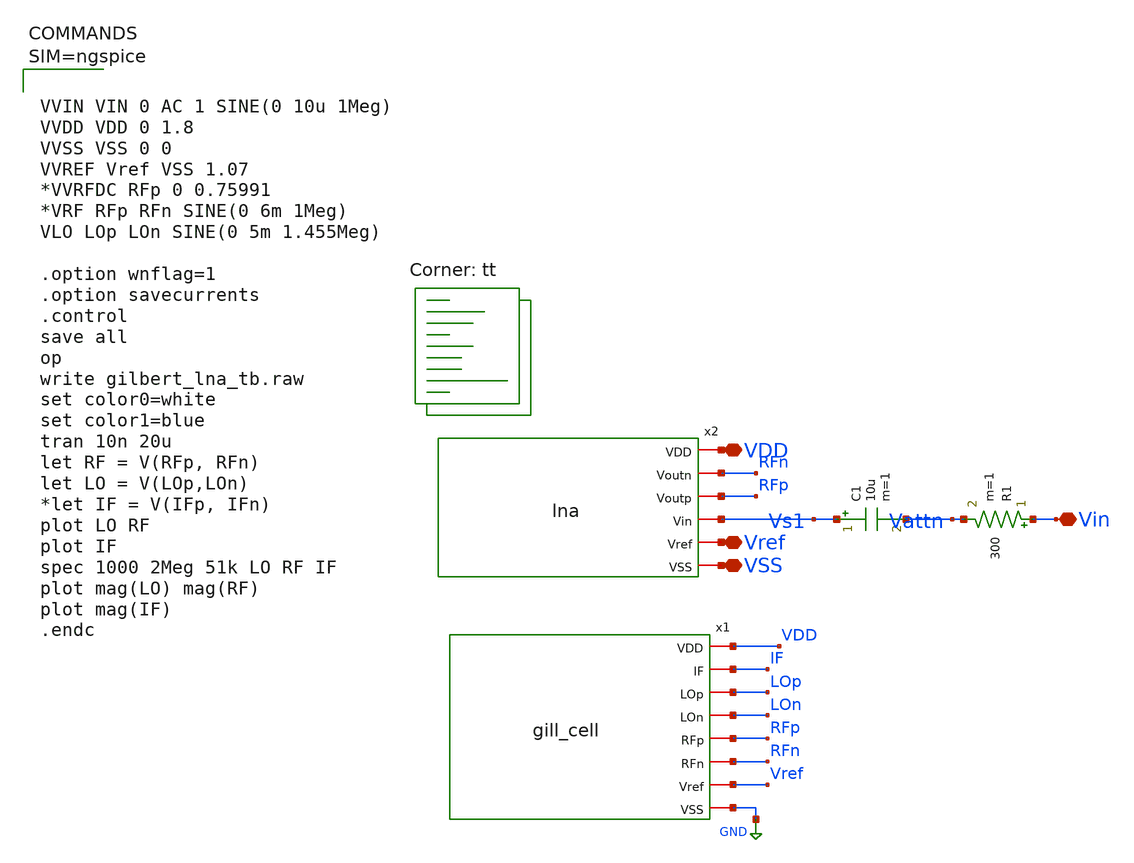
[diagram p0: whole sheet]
** sch_path: Project/xschem/gilbert_lna_tb.sch
**.subckt gilbert_lna_tb VDD Vin Vref VSS
*.iopin VDD
*.iopin Vin
*.iopin Vref
*.iopin VSS
x1 VDD IF LOp LOn RFp RFn Vref GND gill_cell
C1 Vs1 Vattn 10u m=1
R1 Vin Vattn 300 m=1
x2 VDD RFn RFp Vs1 Vref VSS lna
**** begin user architecture code



VVIN VIN 0 AC 1 SINE(0 10u 1Meg)
VVDD VDD 0 1.8
VVSS VSS 0 0
VVREF Vref VSS 1.07
*VVRFDC RFp 0 0.75991
*VRF RFp RFn SINE(0 6m 1Meg)
VLO LOp LOn SINE(0 5m 1.455Meg)

.option wnflag=1
.option savecurrents
.control
save all
op
write gilbert_lna_tb.raw
set color0=white
set color1=blue
tran 10n 20u
let RF = V(RFp, RFn)
let LO = V(LOp,LOn)
*let IF = V(IFp, IFn)
plot LO RF
plot IF
spec 1000 2Meg 51k LO RF IF
plot mag(LO) mag(RF)
plot mag(IF)
.endc



.lib $::SKYWATER_MODELS/sky130.lib.spice tt
**** end user architecture code
**.ends

* expanding   symbol:  gill_cell.sym # of pins=8
** sym_path: Project/xschem/gill_cell.sym
** sch_path: Project/xschem/gill_cell.sch
.subckt gill_cell VDD IF LOp LOn RFp RFn Vref VSS
*.iopin LOp
*.iopin LOn
*.iopin RFp
*.iopin RFn
*.iopin VDD
*.iopin VSS
*.iopin Vref
*.iopin IF
XR1 IF++ VDD VSS sky130_fd_pr__res_xhigh_po_0p69 L=6.9 mult=1 m=1
XR3 IF-- VDD VSS sky130_fd_pr__res_xhigh_po_0p69 L=6.9 mult=1 m=1
XR10 VDD LOp VSS sky130_fd_pr__res_xhigh_po_0p69 L=1.38 mult=1 m=1
XR11 LOp VSS VSS sky130_fd_pr__res_xhigh_po_0p69 L=3.45 mult=1 m=1
XR12 LOn VDD VSS sky130_fd_pr__res_xhigh_po_0p69 L=1.38 mult=1 m=1
XR13 VSS LOn VSS sky130_fd_pr__res_xhigh_po_0p69 L=3.45 mult=1 m=1
XM2 net1 VM VSS VSS sky130_fd_pr__nfet_01v8 L=1.1 W=40 nf=1 ad='int((nf+1)/2) * W/nf * 0.29' as='int((nf+2)/2) * W/nf * 0.29'
+ pd='2*int((nf+1)/2) * (W/nf + 0.29)' ps='2*int((nf+2)/2) * (W/nf + 0.29)' nrd='0.29 / W' nrs='0.29 / W'
+ sa=0 sb=0 sd=0 mult=1 m=1
XM3 Vmid RFp net1 VSS sky130_fd_pr__nfet_01v8 L=1.1 W=40 nf=1 ad='int((nf+1)/2) * W/nf * 0.29' as='int((nf+2)/2) * W/nf * 0.29'
+ pd='2*int((nf+1)/2) * (W/nf + 0.29)' ps='2*int((nf+2)/2) * (W/nf + 0.29)' nrd='0.29 / W' nrs='0.29 / W'
+ sa=0 sb=0 sd=0 mult=1 m=1
XM5 IF++ LOp Vmid VSS sky130_fd_pr__nfet_01v8 L=1.1 W=40 nf=1 ad='int((nf+1)/2) * W/nf * 0.29' as='int((nf+2)/2) * W/nf * 0.29'
+ pd='2*int((nf+1)/2) * (W/nf + 0.29)' ps='2*int((nf+2)/2) * (W/nf + 0.29)' nrd='0.29 / W' nrs='0.29 / W'
+ sa=0 sb=0 sd=0 mult=1 m=1
XM7 IF++ LOn Vmid2 VSS sky130_fd_pr__nfet_01v8 L=1.1 W=40 nf=1 ad='int((nf+1)/2) * W/nf * 0.29' as='int((nf+2)/2) * W/nf * 0.29'
+ pd='2*int((nf+1)/2) * (W/nf + 0.29)' ps='2*int((nf+2)/2) * (W/nf + 0.29)' nrd='0.29 / W' nrs='0.29 / W'
+ sa=0 sb=0 sd=0 mult=1 m=1
XM4 Vmid2 RFn net1 VSS sky130_fd_pr__nfet_01v8 L=1.1 W=40 nf=1 ad='int((nf+1)/2) * W/nf * 0.29' as='int((nf+2)/2) * W/nf * 0.29'
+ pd='2*int((nf+1)/2) * (W/nf + 0.29)' ps='2*int((nf+2)/2) * (W/nf + 0.29)' nrd='0.29 / W' nrs='0.29 / W'
+ sa=0 sb=0 sd=0 mult=1 m=1
XM8 IF-- LOp Vmid2 VSS sky130_fd_pr__nfet_01v8 L=1.1 W=40 nf=1 ad='int((nf+1)/2) * W/nf * 0.29' as='int((nf+2)/2) * W/nf * 0.29'
+ pd='2*int((nf+1)/2) * (W/nf + 0.29)' ps='2*int((nf+2)/2) * (W/nf + 0.29)' nrd='0.29 / W' nrs='0.29 / W'
+ sa=0 sb=0 sd=0 mult=1 m=1
XM6 IF-- LOn Vmid VSS sky130_fd_pr__nfet_01v8 L=1.1 W=40 nf=1 ad='int((nf+1)/2) * W/nf * 0.29' as='int((nf+2)/2) * W/nf * 0.29'
+ pd='2*int((nf+1)/2) * (W/nf + 0.29)' ps='2*int((nf+2)/2) * (W/nf + 0.29)' nrd='0.29 / W' nrs='0.29 / W'
+ sa=0 sb=0 sd=0 mult=1 m=1
XM9 Vamp VM VSS VSS sky130_fd_pr__nfet_01v8 L=1.1 W=40 nf=1 ad='int((nf+1)/2) * W/nf * 0.29' as='int((nf+2)/2) * W/nf * 0.29'
+ pd='2*int((nf+1)/2) * (W/nf + 0.29)' ps='2*int((nf+2)/2) * (W/nf + 0.29)' nrd='0.29 / W' nrs='0.29 / W'
+ sa=0 sb=0 sd=0 mult=1 m=1
XM10 IFn IF++ Vamp VSS sky130_fd_pr__nfet_01v8 L=1.1 W=40 nf=1 ad='int((nf+1)/2) * W/nf * 0.29' as='int((nf+2)/2) * W/nf * 0.29'
+ pd='2*int((nf+1)/2) * (W/nf + 0.29)' ps='2*int((nf+2)/2) * (W/nf + 0.29)' nrd='0.29 / W' nrs='0.29 / W'
+ sa=0 sb=0 sd=0 mult=1 m=1
XM11 IFp IF-- Vamp VSS sky130_fd_pr__nfet_01v8 L=1.1 W=40 nf=1 ad='int((nf+1)/2) * W/nf * 0.29' as='int((nf+2)/2) * W/nf * 0.29'
+ pd='2*int((nf+1)/2) * (W/nf + 0.29)' ps='2*int((nf+2)/2) * (W/nf + 0.29)' nrd='0.29 / W' nrs='0.29 / W'
+ sa=0 sb=0 sd=0 mult=1 m=1
XR14 IFp VDD VSS sky130_fd_pr__res_xhigh_po_0p69 L=9.67 mult=1 m=1
XR15 IFn VDD VSS sky130_fd_pr__res_xhigh_po_0p69 L=9.67 mult=1 m=1
XM1 net2 Vref VSS VSS sky130_fd_pr__nfet_01v8 L=2 W=5 nf=1 ad='int((nf+1)/2) * W/nf * 0.29' as='int((nf+2)/2) * W/nf * 0.29'
+ pd='2*int((nf+1)/2) * (W/nf + 0.29)' ps='2*int((nf+2)/2) * (W/nf + 0.29)' nrd='0.29 / W' nrs='0.29 / W'
+ sa=0 sb=0 sd=0 mult=1 m=1
XM12 VM VM VSS VSS sky130_fd_pr__nfet_01v8 L=2 W=10 nf=1 ad='int((nf+1)/2) * W/nf * 0.29' as='int((nf+2)/2) * W/nf * 0.29'
+ pd='2*int((nf+1)/2) * (W/nf + 0.29)' ps='2*int((nf+2)/2) * (W/nf + 0.29)' nrd='0.29 / W' nrs='0.29 / W'
+ sa=0 sb=0 sd=0 mult=1 m=1
XM15 VM net2 VDD VDD sky130_fd_pr__pfet_01v8 L=8 W=5 nf=1 ad='int((nf+1)/2) * W/nf * 0.29' as='int((nf+2)/2) * W/nf * 0.29'
+ pd='2*int((nf+1)/2) * (W/nf + 0.29)' ps='2*int((nf+2)/2) * (W/nf + 0.29)' nrd='0.29 / W' nrs='0.29 / W'
+ sa=0 sb=0 sd=0 mult=1 m=1
XM13 net2 net2 VDD VDD sky130_fd_pr__pfet_01v8 L=8 W=5 nf=1 ad='int((nf+1)/2) * W/nf * 0.29' as='int((nf+2)/2) * W/nf * 0.29'
+ pd='2*int((nf+1)/2) * (W/nf + 0.29)' ps='2*int((nf+2)/2) * (W/nf + 0.29)' nrd='0.29 / W' nrs='0.29 / W'
+ sa=0 sb=0 sd=0 mult=1 m=1
XM14 IF IFp VSS VSS sky130_fd_pr__nfet_01v8 L=1 W=40 nf=1 ad='int((nf+1)/2) * W/nf * 0.29' as='int((nf+2)/2) * W/nf * 0.29'
+ pd='2*int((nf+1)/2) * (W/nf + 0.29)' ps='2*int((nf+2)/2) * (W/nf + 0.29)' nrd='0.29 / W' nrs='0.29 / W'
+ sa=0 sb=0 sd=0 mult=1 m=1
XM16 VDD Vref IF VSS sky130_fd_pr__nfet_01v8 L=1 W=40 nf=1 ad='int((nf+1)/2) * W/nf * 0.29' as='int((nf+2)/2) * W/nf * 0.29'
+ pd='2*int((nf+1)/2) * (W/nf + 0.29)' ps='2*int((nf+2)/2) * (W/nf + 0.29)' nrd='0.29 / W' nrs='0.29 / W'
+ sa=0 sb=0 sd=0 mult=1 m=1
.ends


* expanding   symbol:  /home/renslow/Documents/ece5120/hw06/xschem/lna.sym # of pins=6
** sym_path: Project/xschem/lna.sym
** sch_path: Project/xschem/lna.sch
.subckt lna VDD Voutn Voutp Vin Vref VSS
*.iopin VSS
*.iopin VDD
*.iopin Voutp
*.iopin Voutn
*.iopin Vref
*.iopin Vin
XR1 Vg VDD VSS sky130_fd_pr__res_xhigh_po_5p73 L=10 mult=1 m=1
XR2 VSS Vg VSS sky130_fd_pr__res_xhigh_po_5p73 L=20 mult=1 m=1
XM1 Vg2 Vg Vin VSS sky130_fd_pr__nfet_01v8 L=1 W=70 nf=1 ad='int((nf+1)/2) * W/nf * 0.29' as='int((nf+2)/2) * W/nf * 0.29'
+ pd='2*int((nf+1)/2) * (W/nf + 0.29)' ps='2*int((nf+2)/2) * (W/nf + 0.29)' nrd='0.29 / W' nrs='0.29 / W'
+ sa=0 sb=0 sd=0 mult=1 m=1
XM2 Vin Vref VSS VSS sky130_fd_pr__nfet_01v8 L=1 W=10 nf=1 ad='int((nf+1)/2) * W/nf * 0.29' as='int((nf+2)/2) * W/nf * 0.29'
+ pd='2*int((nf+1)/2) * (W/nf + 0.29)' ps='2*int((nf+2)/2) * (W/nf + 0.29)' nrd='0.29 / W' nrs='0.29 / W'
+ sa=0 sb=0 sd=0 mult=1 m=1
XM3 Vs Vref VSS VSS sky130_fd_pr__nfet_01v8 L=1 W=3 nf=1 ad='int((nf+1)/2) * W/nf * 0.29' as='int((nf+2)/2) * W/nf * 0.29'
+ pd='2*int((nf+1)/2) * (W/nf + 0.29)' ps='2*int((nf+2)/2) * (W/nf + 0.29)' nrd='0.29 / W' nrs='0.29 / W'
+ sa=0 sb=0 sd=0 mult=1 m=1
XM4 Voutn Vg2 Vs VSS sky130_fd_pr__nfet_01v8 L=1 W=40 nf=1 ad='int((nf+1)/2) * W/nf * 0.29' as='int((nf+2)/2) * W/nf * 0.29'
+ pd='2*int((nf+1)/2) * (W/nf + 0.29)' ps='2*int((nf+2)/2) * (W/nf + 0.29)' nrd='0.29 / W' nrs='0.29 / W'
+ sa=0 sb=0 sd=0 mult=1 m=1
XM5 Voutp Vg3 Vs VSS sky130_fd_pr__nfet_01v8 L=1 W=40 nf=1 ad='int((nf+1)/2) * W/nf * 0.29' as='int((nf+2)/2) * W/nf * 0.29'
+ pd='2*int((nf+1)/2) * (W/nf + 0.29)' ps='2*int((nf+2)/2) * (W/nf + 0.29)' nrd='0.29 / W' nrs='0.29 / W'
+ sa=0 sb=0 sd=0 mult=1 m=1
XR3 Vg2 VDD VSS sky130_fd_pr__res_xhigh_po_5p73 L=12 mult=1 m=1
XM8 Voutp Voutn VDD VDD sky130_fd_pr__pfet_01v8 L=1 W=40 nf=1 ad='int((nf+1)/2) * W/nf * 0.29' as='int((nf+2)/2) * W/nf * 0.29'
+ pd='2*int((nf+1)/2) * (W/nf + 0.29)' ps='2*int((nf+2)/2) * (W/nf + 0.29)' nrd='0.29 / W' nrs='0.29 / W'
+ sa=0 sb=0 sd=0 mult=1 m=1
XM6 Voutn Voutn VDD VDD sky130_fd_pr__pfet_01v8 L=1 W=40 nf=1 ad='int((nf+1)/2) * W/nf * 0.29' as='int((nf+2)/2) * W/nf * 0.29'
+ pd='2*int((nf+1)/2) * (W/nf + 0.29)' ps='2*int((nf+2)/2) * (W/nf + 0.29)' nrd='0.29 / W' nrs='0.29 / W'
+ sa=0 sb=0 sd=0 mult=1 m=1
XC1 Vg3 VSS sky130_fd_pr__cap_mim_m3_1 W=30 L=30 MF=1 m=1
XC2 Vg3 VSS sky130_fd_pr__cap_mim_m3_1 W=30 L=30 MF=1 m=1
XR4 Vg2 Vg3 VSS sky130_fd_pr__res_xhigh_po_0p35 L=39.26 mult=1 m=1
.ends

.GLOBAL GND
.end
